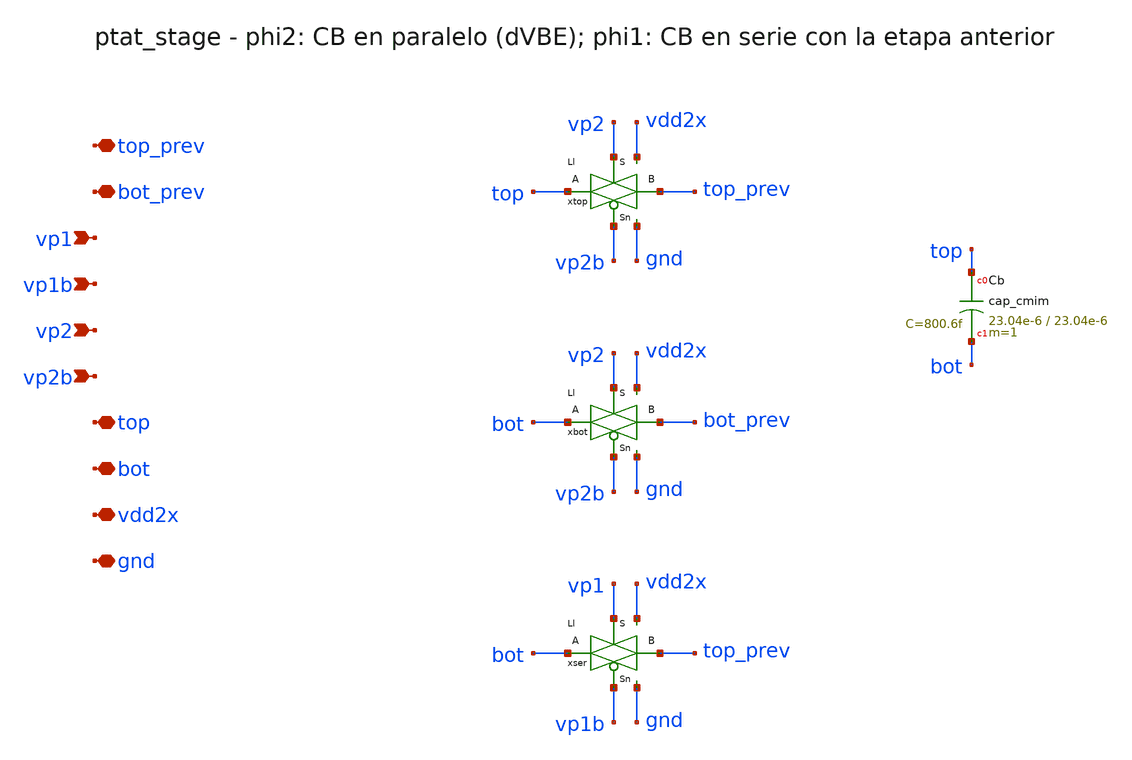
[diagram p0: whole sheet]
** sch_path: Enfoque_A/xschem/celdas/ptat_stage.sch
**.subckt ptat_stage top_prev bot_prev vp1 vp1b vp2 vp2b top bot vdd2x gnd
*.iopin top_prev
*.iopin bot_prev
*.ipin vp1
*.ipin vp1b
*.ipin vp2
*.ipin vp2b
*.iopin top
*.iopin bot
*.iopin vdd2x
*.iopin gnd
xtop top top_prev vp2 vp2b vdd2x gnd Ll
xbot bot bot_prev vp2 vp2b vdd2x gnd Ll
xser bot top_prev vp1 vp1b vdd2x gnd Ll
XCb top bot cap_cmim w=23.04e-6 l=23.04e-6 m=1 mm_ok=1
**.ends

* expanding   symbol:  Enfoque_A/xschem/celdas/Ll.sym # of pins=6
** sym_path: Enfoque_A/xschem/celdas/Ll.sym
** sch_path: Enfoque_A/xschem/celdas/Ll.sch
.subckt Ll A B S Sn vdd gnd
*.iopin gnd
*.iopin vdd
*.iopin B
*.ipin Sn
*.ipin S
*.iopin A
XM101 A S B gnd sg13_lv_nmos w=0.13u l=0.130u ng=1 m=1 mm_ok=1
XM100 B Sn A vdd sg13_lv_pmos w=0.3u l=0.130u ng=1 m=1 mm_ok=1
.ends

.end
